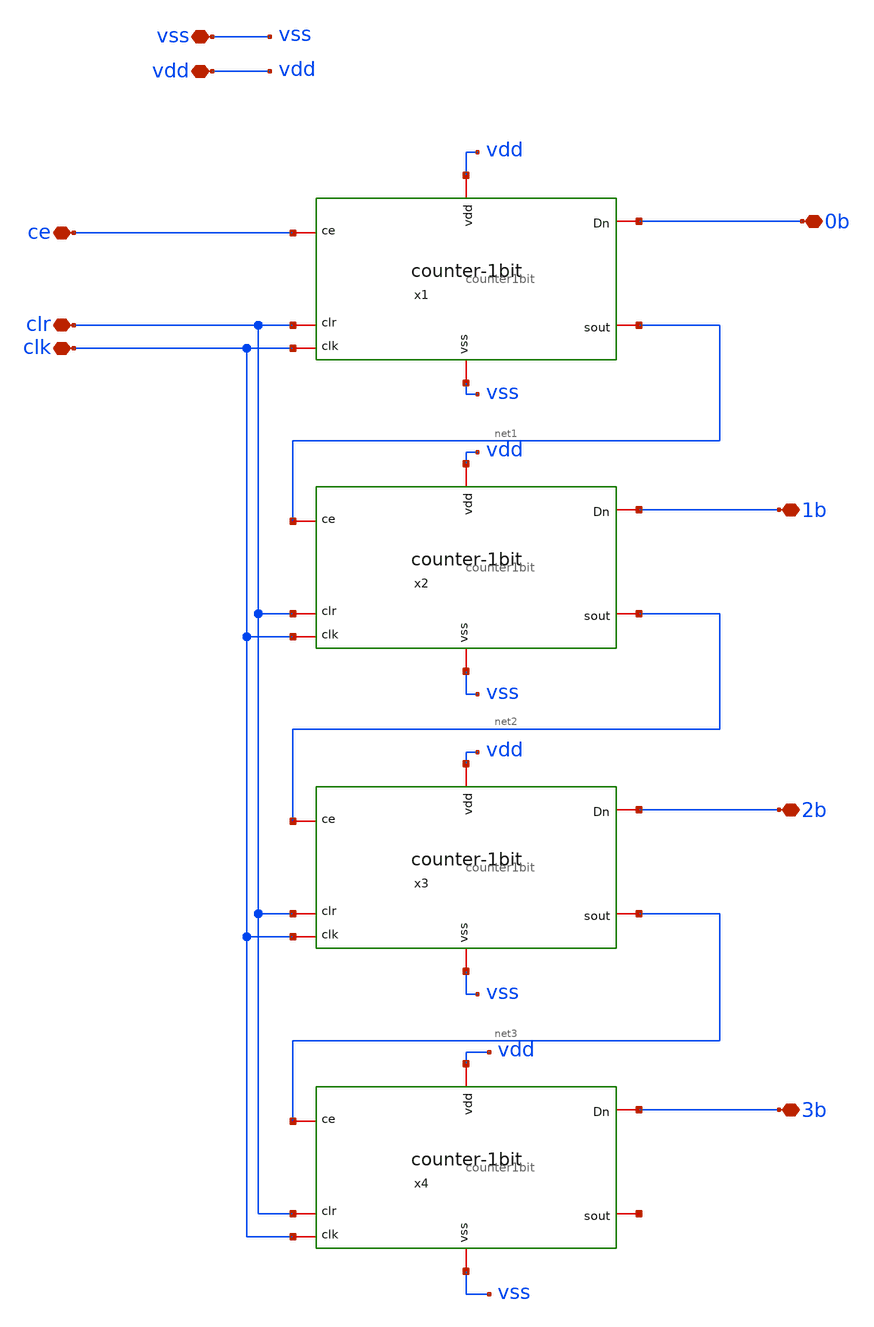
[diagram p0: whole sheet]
** sch_path: design/counter4bits.sch
**.subckt counter4bits vdd vss ce clr clk 0b 1b 2b 3b
*.iopin vdd
*.iopin vss
*.iopin ce
*.iopin clr
*.iopin clk
*.iopin 0b
*.iopin 1b
*.iopin 2b
*.iopin 3b
x1 clr 0b ce clk vss vdd net1 counter1bit
x2 clr 1b net1 clk vss vdd net2 counter1bit
x3 clr 2b net2 clk vss vdd net3 counter1bit
x4 clr 3b net3 clk vss vdd net4 counter1bit
**.ends
.end
